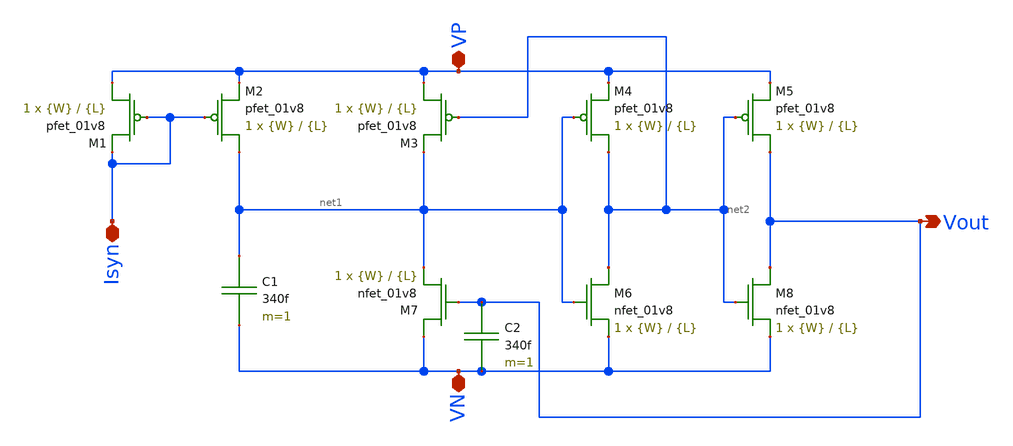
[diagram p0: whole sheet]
** sch_path: schematic/besrour_neuron.sch
**.subckt besrour_neuron Vout VP VN Isyn
*.opin Vout
*.iopin VP
*.iopin VN
*.iopin Isyn
XM1 VP Isyn Isyn VDD sky130_fd_pr__pfet_01v8 L={L} W={W} nf=1 ad='int((nf+1)/2) * W/nf * 0.29' as='int((nf+2)/2) * W/nf * 0.29'
+ pd='2*int((nf+1)/2) * (W/nf + 0.29)' ps='2*int((nf+2)/2) * (W/nf + 0.29)' nrd='0.29 / W' nrs='0.29 / W'
+ sa=0 sb=0 sd=0 mult=1 m=1
XM7 VN Vout net1 GND sky130_fd_pr__nfet_01v8 L={L} W={W} nf=1 ad='int((nf+1)/2) * W/nf * 0.29' as='int((nf+2)/2) * W/nf * 0.29'
+ pd='2*int((nf+1)/2) * (W/nf + 0.29)' ps='2*int((nf+2)/2) * (W/nf + 0.29)' nrd='0.29 / W' nrs='0.29 / W'
+ sa=0 sb=0 sd=0 mult=1 m=1
XM2 net1 Isyn VP VDD sky130_fd_pr__pfet_01v8 L={L} W={W} nf=1 ad='int((nf+1)/2) * W/nf * 0.29' as='int((nf+2)/2) * W/nf * 0.29'
+ pd='2*int((nf+1)/2) * (W/nf + 0.29)' ps='2*int((nf+2)/2) * (W/nf + 0.29)' nrd='0.29 / W' nrs='0.29 / W'
+ sa=0 sb=0 sd=0 mult=1 m=1
XM3 VP net2 net1 VDD sky130_fd_pr__pfet_01v8 L={L} W={W} nf=1 ad='int((nf+1)/2) * W/nf * 0.29' as='int((nf+2)/2) * W/nf * 0.29'
+ pd='2*int((nf+1)/2) * (W/nf + 0.29)' ps='2*int((nf+2)/2) * (W/nf + 0.29)' nrd='0.29 / W' nrs='0.29 / W'
+ sa=0 sb=0 sd=0 mult=1 m=1
XM4 net2 net1 VP VDD sky130_fd_pr__pfet_01v8 L={L} W={W} nf=1 ad='int((nf+1)/2) * W/nf * 0.29' as='int((nf+2)/2) * W/nf * 0.29'
+ pd='2*int((nf+1)/2) * (W/nf + 0.29)' ps='2*int((nf+2)/2) * (W/nf + 0.29)' nrd='0.29 / W' nrs='0.29 / W'
+ sa=0 sb=0 sd=0 mult=1 m=1
XM5 Vout net2 VP VDD sky130_fd_pr__pfet_01v8 L={L} W={W} nf=1 ad='int((nf+1)/2) * W/nf * 0.29' as='int((nf+2)/2) * W/nf * 0.29'
+ pd='2*int((nf+1)/2) * (W/nf + 0.29)' ps='2*int((nf+2)/2) * (W/nf + 0.29)' nrd='0.29 / W' nrs='0.29 / W'
+ sa=0 sb=0 sd=0 mult=1 m=1
XM6 net2 net1 VN GND sky130_fd_pr__nfet_01v8 L={L} W={W} nf=1 ad='int((nf+1)/2) * W/nf * 0.29' as='int((nf+2)/2) * W/nf * 0.29'
+ pd='2*int((nf+1)/2) * (W/nf + 0.29)' ps='2*int((nf+2)/2) * (W/nf + 0.29)' nrd='0.29 / W' nrs='0.29 / W'
+ sa=0 sb=0 sd=0 mult=1 m=1
XM8 Vout net2 VN GND sky130_fd_pr__nfet_01v8 L={L} W={W} nf=1 ad='int((nf+1)/2) * W/nf * 0.29' as='int((nf+2)/2) * W/nf * 0.29'
+ pd='2*int((nf+1)/2) * (W/nf + 0.29)' ps='2*int((nf+2)/2) * (W/nf + 0.29)' nrd='0.29 / W' nrs='0.29 / W'
+ sa=0 sb=0 sd=0 mult=1 m=1
C1 net1 VN 340f m=1
C2 Vout VN 340f m=1
**.ends
.end
